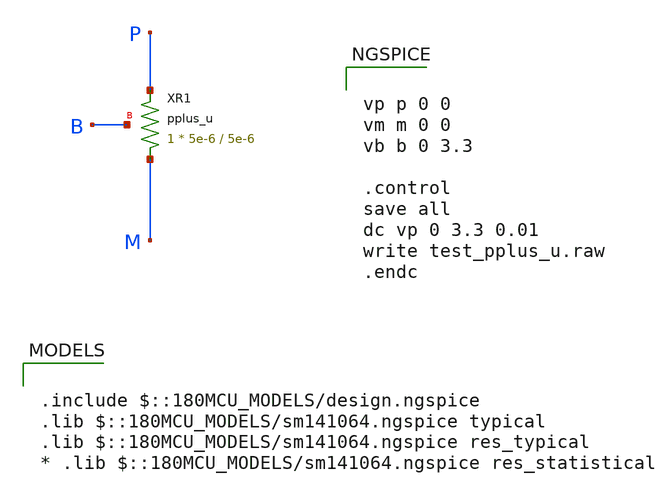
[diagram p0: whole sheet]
** sch_path: gf180mcuD/xschem_libs/gf180mcu_tests/test_pplus_u/schematic/test_pplus_u.sch
* Copyright 2022 GlobalFoundries PDK Authors
* Licensed under the Apache License, Version 2.0 (the "License");
* you may not use this file except in compliance with the License.
* You may obtain a copy of the License at
* https://www.apache.org/licenses/LICENSE-2.0
* Unless required by applicable law or agreed to in writing, software
* distributed under the License is distributed on an "AS IS" BASIS,
* WITHOUT WARRANTIES OR CONDITIONS OF ANY KIND, either express or implied.
* See the License for the specific language governing permissions and
* limitations under the License.
**.subckt test_pplus_u
XR1 M P B pplus_u r_width=5e-6 r_length=5e-6 m=1
**** begin user architecture code

.include $::180MCU_MODELS/design.ngspice
.lib $::180MCU_MODELS/sm141064.ngspice typical
.lib $::180MCU_MODELS/sm141064.ngspice res_typical
* .lib $::180MCU_MODELS/sm141064.ngspice res_statistical



vp p 0 0
vm m 0 0
vb b 0 3.3

.control
save all
dc vp 0 3.3 0.01
write test_pplus_u.raw
.endc


**** end user architecture code
**.ends
.end
